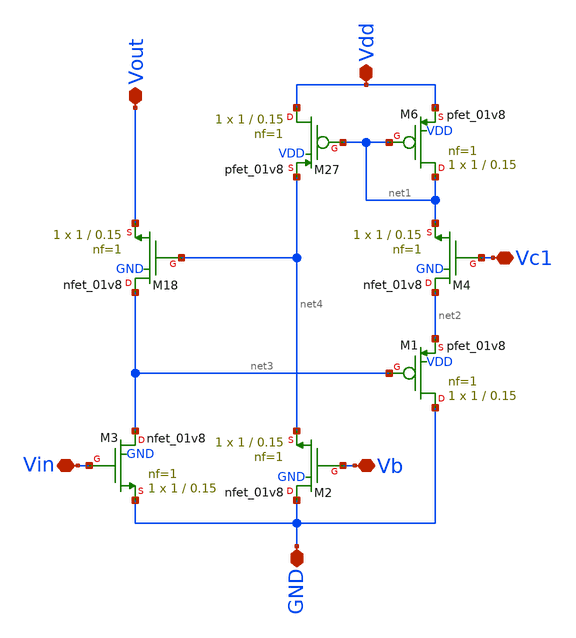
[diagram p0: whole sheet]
** sch_path: triode.sch
**.subckt triode Vout Vc1 Vb Vin GND Vdd
*.iopin Vout
*.iopin Vc1
*.iopin Vb
*.iopin Vin
*.iopin GND
*.iopin Vdd
XM27 Vdd net1 net4 VDD sky130_fd_pr__pfet_01v8 L=0.15 W=1 nf=1 ad='int((1 + 1)/2) * 1 / 1 * 0.29' as='int((1 + 2)/2) * 1 / 1 * 0.29'
+ pd='2*int((1 + 1)/2) * (1 / 1 + 0.29)' ps='2*int((1 + 2)/2) * (1 / 1 + 0.29)' nrd='0.29 / 1 ' nrs='0.29 / 1 '
+ sa=0 sb=0 sd=0 mult=1 m=1
XM6 net1 net1 Vdd VDD sky130_fd_pr__pfet_01v8 L=0.15 W=1 nf=1 ad='int((1 + 1)/2) * 1 / 1 * 0.29' as='int((1 + 2)/2) * 1 / 1 * 0.29'
+ pd='2*int((1 + 1)/2) * (1 / 1 + 0.29)' ps='2*int((1 + 2)/2) * (1 / 1 + 0.29)' nrd='0.29 / 1 ' nrs='0.29 / 1 '
+ sa=0 sb=0 sd=0 mult=1 m=1
XM18 net3 net4 Vout GND sky130_fd_pr__nfet_01v8 L=0.15 W=1 nf=1 ad='int((nf+1)/2) * W/nf * 0.29' as='int((nf+2)/2) * W/nf * 0.29'
+ pd='2*int((nf+1)/2) * (W/nf + 0.29)' ps='2*int((nf+2)/2) * (W/nf + 0.29)' nrd='0.29 / W' nrs='0.29 / W'
+ sa=0 sb=0 sd=0 mult=1 m=1
XM3 net3 Vin GND GND sky130_fd_pr__nfet_01v8 L=0.15 W=1 nf=1 ad='int((nf+1)/2) * W/nf * 0.29' as='int((nf+2)/2) * W/nf * 0.29'
+ pd='2*int((nf+1)/2) * (W/nf + 0.29)' ps='2*int((nf+2)/2) * (W/nf + 0.29)' nrd='0.29 / W' nrs='0.29 / W'
+ sa=0 sb=0 sd=0 mult=1 m=1
XM2 GND Vb net4 GND sky130_fd_pr__nfet_01v8 L=0.15 W=1 nf=1 ad='int((nf+1)/2) * W/nf * 0.29' as='int((nf+2)/2) * W/nf * 0.29'
+ pd='2*int((nf+1)/2) * (W/nf + 0.29)' ps='2*int((nf+2)/2) * (W/nf + 0.29)' nrd='0.29 / W' nrs='0.29 / W'
+ sa=0 sb=0 sd=0 mult=1 m=1
XM4 net2 Vc1 net1 GND sky130_fd_pr__nfet_01v8 L=0.15 W=1 nf=1 ad='int((nf+1)/2) * W/nf * 0.29' as='int((nf+2)/2) * W/nf * 0.29'
+ pd='2*int((nf+1)/2) * (W/nf + 0.29)' ps='2*int((nf+2)/2) * (W/nf + 0.29)' nrd='0.29 / W' nrs='0.29 / W'
+ sa=0 sb=0 sd=0 mult=1 m=1
XM1 GND net3 net2 VDD sky130_fd_pr__pfet_01v8 L=0.15 W=1 nf=1 ad='int((1 + 1)/2) * 1 / 1 * 0.29' as='int((1 + 2)/2) * 1 / 1 * 0.29'
+ pd='2*int((1 + 1)/2) * (1 / 1 + 0.29)' ps='2*int((1 + 2)/2) * (1 / 1 + 0.29)' nrd='0.29 / 1 ' nrs='0.29 / 1 '
+ sa=0 sb=0 sd=0 mult=1 m=1
**.ends
.end
